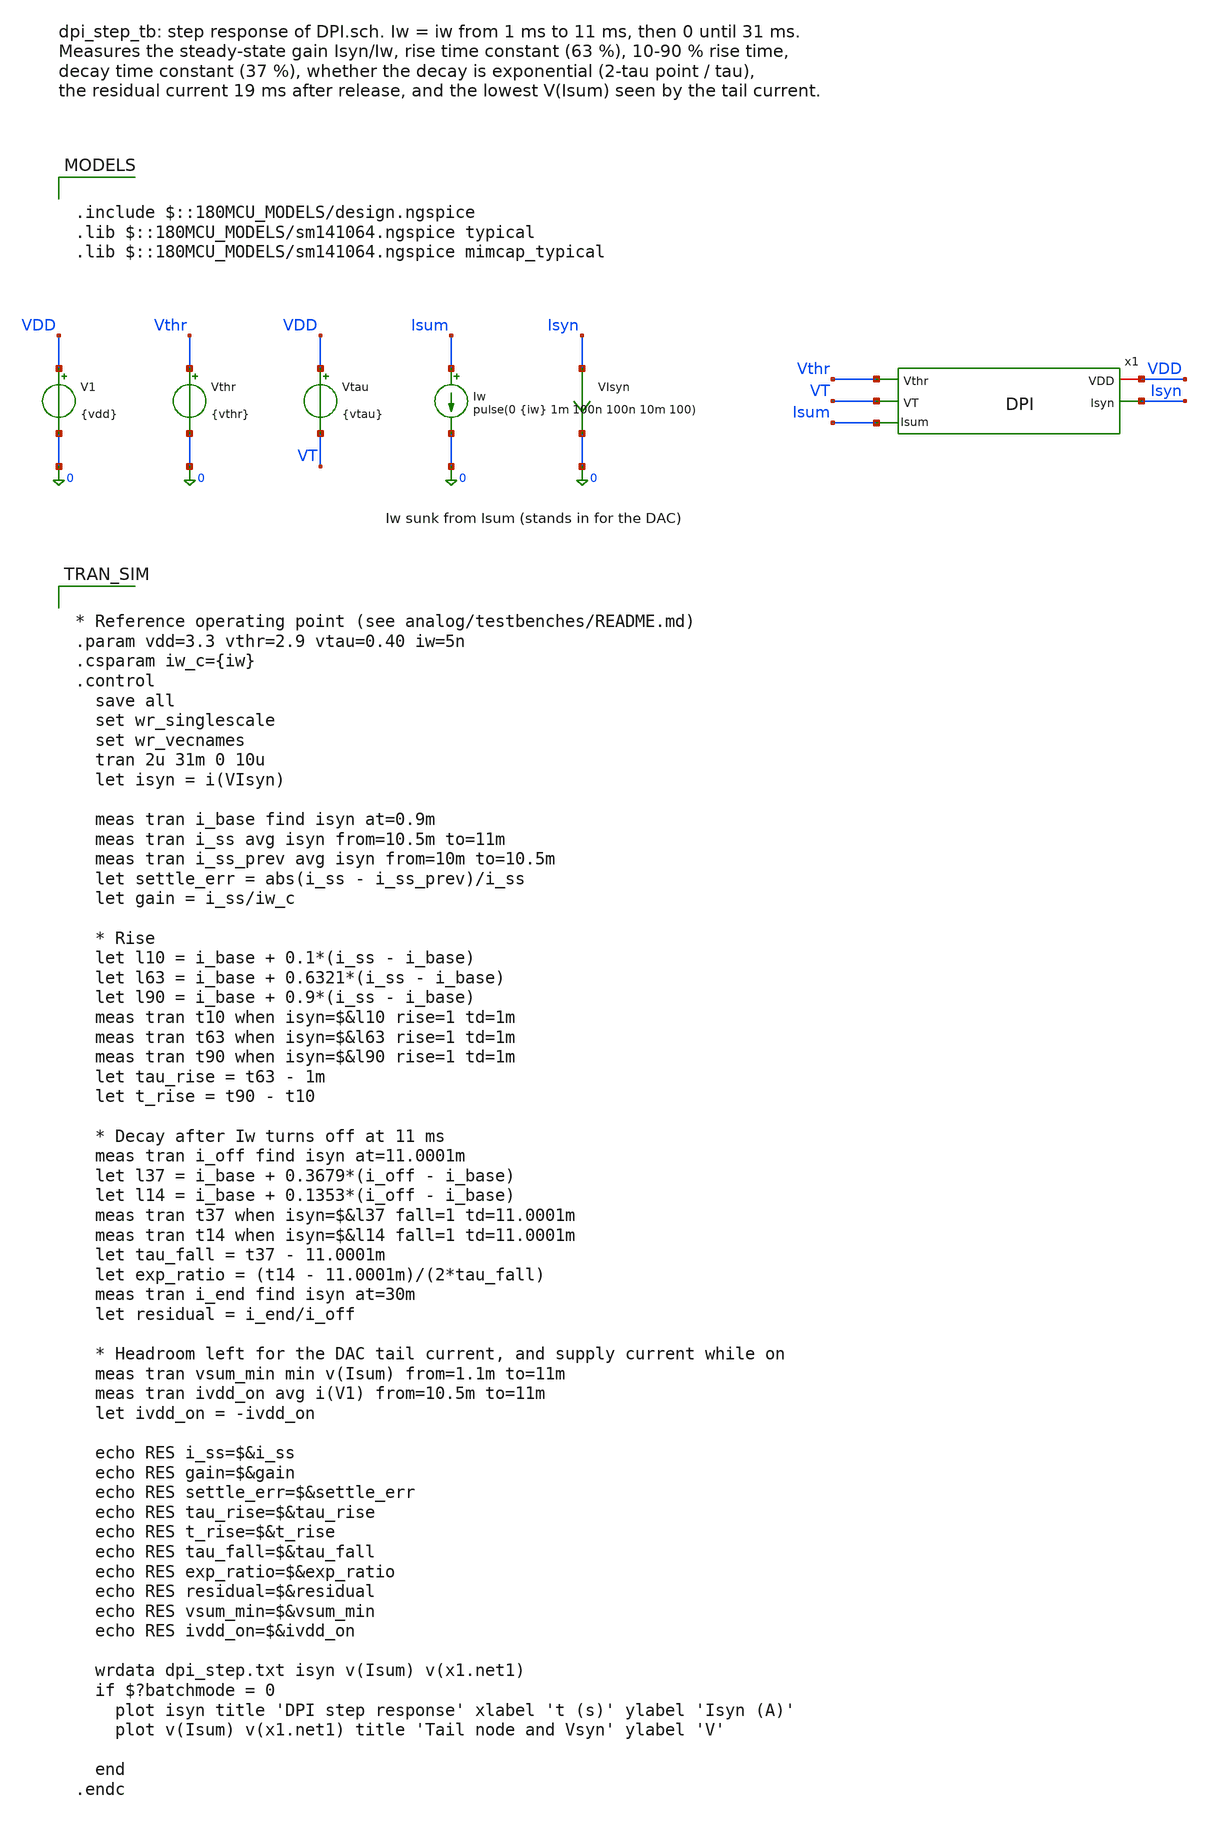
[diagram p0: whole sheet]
** sch_path: analog/testbenches/dpi/dpi_step_tb.sch
**.subckt dpi_step_tb
V1 VDD 0 {vdd}
Vthr Vthr 0 {vthr}
Vtau VDD VT {vtau}
Iw Isum 0 pulse(0 {iw} 1m 100n 100n 10m 100)
VIsyn Isyn 0 0
.save i(visyn)
x1 VDD Vthr Isyn Isum VT DPI
**** begin user architecture code


* Reference operating point (see analog/testbenches/README.md)
.param vdd=3.3 vthr=2.9 vtau=0.40 iw=5n
.csparam iw_c={iw}
.control
  save all
  set wr_singlescale
  set wr_vecnames
  tran 2u 31m 0 10u
  let isyn = i(VIsyn)

  meas tran i_base find isyn at=0.9m
  meas tran i_ss avg isyn from=10.5m to=11m
  meas tran i_ss_prev avg isyn from=10m to=10.5m
  let settle_err = abs(i_ss - i_ss_prev)/i_ss
  let gain = i_ss/iw_c

  * Rise
  let l10 = i_base + 0.1*(i_ss - i_base)
  let l63 = i_base + 0.6321*(i_ss - i_base)
  let l90 = i_base + 0.9*(i_ss - i_base)
  meas tran t10 when isyn=$&l10 rise=1 td=1m
  meas tran t63 when isyn=$&l63 rise=1 td=1m
  meas tran t90 when isyn=$&l90 rise=1 td=1m
  let tau_rise = t63 - 1m
  let t_rise = t90 - t10

  * Decay after Iw turns off at 11 ms
  meas tran i_off find isyn at=11.0001m
  let l37 = i_base + 0.3679*(i_off - i_base)
  let l14 = i_base + 0.1353*(i_off - i_base)
  meas tran t37 when isyn=$&l37 fall=1 td=11.0001m
  meas tran t14 when isyn=$&l14 fall=1 td=11.0001m
  let tau_fall = t37 - 11.0001m
  let exp_ratio = (t14 - 11.0001m)/(2*tau_fall)
  meas tran i_end find isyn at=30m
  let residual = i_end/i_off

  * Headroom left for the DAC tail current, and supply current while on
  meas tran vsum_min min v(Isum) from=1.1m to=11m
  meas tran ivdd_on avg i(V1) from=10.5m to=11m
  let ivdd_on = -ivdd_on

  echo RES i_ss=$&i_ss
  echo RES gain=$&gain
  echo RES settle_err=$&settle_err
  echo RES tau_rise=$&tau_rise
  echo RES t_rise=$&t_rise
  echo RES tau_fall=$&tau_fall
  echo RES exp_ratio=$&exp_ratio
  echo RES residual=$&residual
  echo RES vsum_min=$&vsum_min
  echo RES ivdd_on=$&ivdd_on

  wrdata dpi_step.txt isyn v(Isum) v(x1.net1)
  if $?batchmode = 0
    plot isyn title 'DPI step response' xlabel 't (s)' ylabel 'Isyn (A)'
    plot v(Isum) v(x1.net1) title 'Tail node and Vsyn' ylabel 'V'

  end
.endc



.include $::180MCU_MODELS/design.ngspice
.lib $::180MCU_MODELS/sm141064.ngspice typical
.lib $::180MCU_MODELS/sm141064.ngspice mimcap_typical

**** end user architecture code
**.ends

* expanding   symbol:  DPI.sym # of pins=5
** sym_path: analog/neuron/DPI.sym
** sch_path: analog/neuron/DPI.sch
.subckt DPI VDD Vthr Isyn Isum VT
*.ipin Vthr
*.iopin VDD
*.opin Isyn
*.opin Isum
*.ipin VT
XM1 VDD Vthr Isum Isum nfet_03v3 L=0.28u W=0.22u nf=1 ad='int((nf+1)/2) * W/nf * 0.18u' as='int((nf+2)/2) * W/nf * 0.18u'
+ pd='2*int((nf+1)/2) * (W/nf + 0.18u)' ps='2*int((nf+2)/2) * (W/nf + 0.18u)' nrd='0.18u / W' nrs='0.18u / W'
+ sa=0 sb=0 sd=0 m=1
XM2 net1 net1 Isum Isum nfet_03v3 L=0.28u W=0.22u nf=1 ad='int((nf+1)/2) * W/nf * 0.18u' as='int((nf+2)/2) * W/nf * 0.18u'
+ pd='2*int((nf+1)/2) * (W/nf + 0.18u)' ps='2*int((nf+2)/2) * (W/nf + 0.18u)' nrd='0.18u / W' nrs='0.18u / W'
+ sa=0 sb=0 sd=0 m=1
XM3 net1 VT VDD VDD pfet_03v3 L=0.28u W=0.22u nf=1 ad='int((nf+1)/2) * W/nf * 0.18u' as='int((nf+2)/2) * W/nf * 0.18u'
+ pd='2*int((nf+1)/2) * (W/nf + 0.18u)' ps='2*int((nf+2)/2) * (W/nf + 0.18u)' nrd='0.18u / W' nrs='0.18u / W'
+ sa=0 sb=0 sd=0 m=1
XM4 Isyn net1 VDD VDD pfet_03v3 L=0.28u W=0.22u nf=1 ad='int((nf+1)/2) * W/nf * 0.18u' as='int((nf+2)/2) * W/nf * 0.18u'
+ pd='2*int((nf+1)/2) * (W/nf + 0.18u)' ps='2*int((nf+2)/2) * (W/nf + 0.18u)' nrd='0.18u / W' nrs='0.18u / W'
+ sa=0 sb=0 sd=0 m=1
C4 VDD net1 1p m=1
.ends

.end
